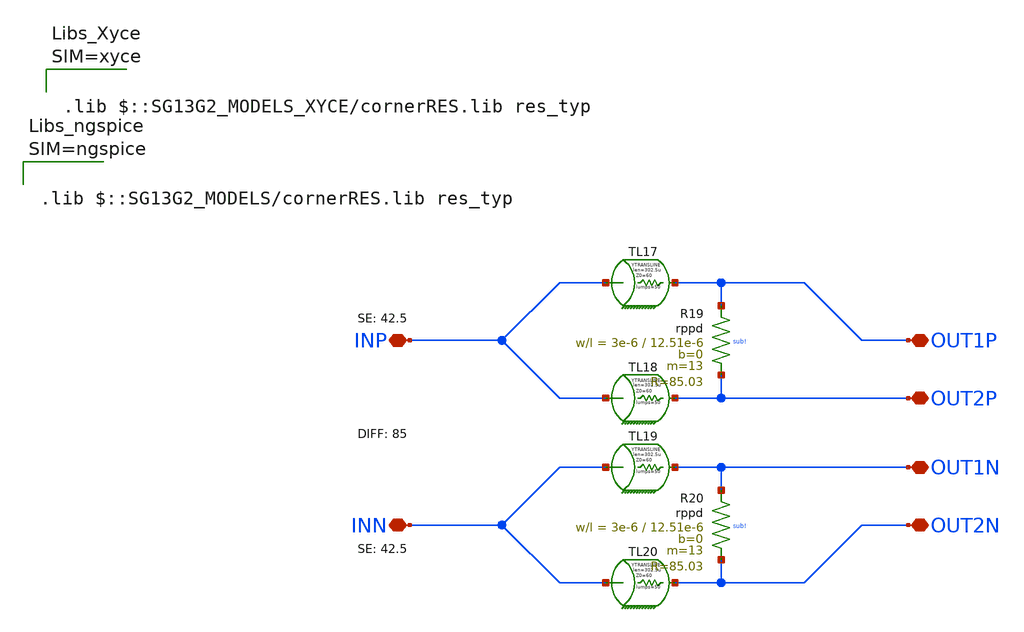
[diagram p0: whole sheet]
** sch_path: mWATTBAT/design_data/xschem/WILKINSON.sch
**.subckt WILKINSON INP INN OUT1P OUT2N OUT1N OUT2P
*.iopin INP
*.iopin INN
*.iopin OUT1P
*.iopin OUT2N
*.iopin OUT1N
*.iopin OUT2P
ytransline TL17 INP OUT1P ytransline_TL17 len=302.5u lumps=50
.model ytransline_TL17 transline r=13.55k l=331.35n C=91.75p
ytransline TL18 INP OUT2P ytransline_TL18 len=302.5u lumps=50
.model ytransline_TL18 transline r=13.55k l=331.35n C=91.75p
ytransline TL19 INN OUT1N ytransline_TL19 len=302.5u lumps=50
.model ytransline_TL19 transline r=13.55k l=331.35n C=91.75p
ytransline TL20 INN OUT2N ytransline_TL20 len=302.5u lumps=50
.model ytransline_TL20 transline r=13.55k l=331.35n C=91.75p
XR19 OUT1P OUT2P sub! rppd w=3e-6 l=12.51e-6 m=13 b=0 mm_ok=1
XR20 OUT1N OUT2N sub! rppd w=3e-6 l=12.51e-6 m=13 b=0 mm_ok=1
**** begin user architecture code






.lib $::SG13G2_MODELS/cornerRES.lib res_typ



**** end user architecture code
**.ends
.end
